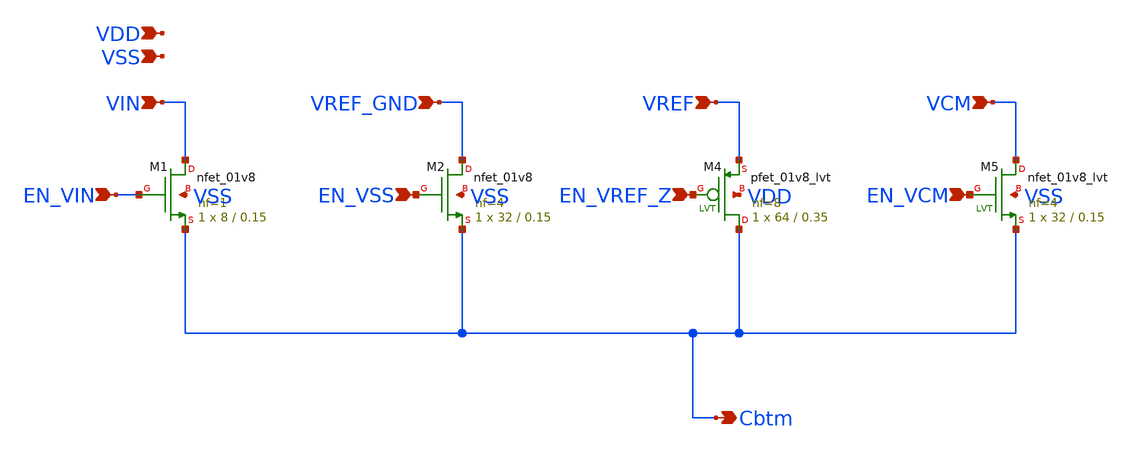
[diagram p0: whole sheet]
** sch_path: individual_switches/switch_C9.sch
**.subckt switch_C9 VIN EN_VIN VREF_GND VREF VCM EN_VCM Cbtm VDD EN_VSS EN_VREF_Z VSS
*.ipin VIN
*.ipin EN_VIN
*.ipin VREF_GND
*.ipin VREF
*.ipin VCM
*.ipin EN_VCM
*.opin Cbtm
*.ipin VDD
*.ipin EN_VSS
*.ipin EN_VREF_Z
*.ipin VSS
XM1 VIN EN_VIN Cbtm VSS sky130_fd_pr__nfet_01v8 L=0.15 W=8 nf=1 ad='int((nf+1)/2) * W/nf * 0.29' as='int((nf+2)/2) * W/nf * 0.29'
+ pd='2*int((nf+1)/2) * (W/nf + 0.29)' ps='2*int((nf+2)/2) * (W/nf + 0.29)' nrd='0.29 / W' nrs='0.29 / W'
+ sa=0 sb=0 sd=0 mult=1 m=1
XM2 VREF_GND EN_VSS Cbtm VSS sky130_fd_pr__nfet_01v8 L=0.15 W=32 nf=4 ad='int((nf+1)/2) * W/nf * 0.29'
+ as='int((nf+2)/2) * W/nf * 0.29' pd='2*int((nf+1)/2) * (W/nf + 0.29)' ps='2*int((nf+2)/2) * (W/nf + 0.29)'
+ nrd='0.29 / W' nrs='0.29 / W' sa=0 sb=0 sd=0 mult=1 m=1
XM4 Cbtm EN_VREF_Z VREF VDD sky130_fd_pr__pfet_01v8_lvt L=0.35 W=64 nf=8 ad='int((nf+1)/2) * W/nf * 0.29'
+ as='int((nf+2)/2) * W/nf * 0.29' pd='2*int((nf+1)/2) * (W/nf + 0.29)' ps='2*int((nf+2)/2) * (W/nf + 0.29)'
+ nrd='0.29 / W' nrs='0.29 / W' sa=0 sb=0 sd=0 mult=1 m=1
XM5 VCM EN_VCM Cbtm VSS sky130_fd_pr__nfet_01v8_lvt L=0.15 W=32 nf=4 ad='int((nf+1)/2) * W/nf * 0.29'
+ as='int((nf+2)/2) * W/nf * 0.29' pd='2*int((nf+1)/2) * (W/nf + 0.29)' ps='2*int((nf+2)/2) * (W/nf + 0.29)'
+ nrd='0.29 / W' nrs='0.29 / W' sa=0 sb=0 sd=0 mult=1 m=1
**.ends
.end
